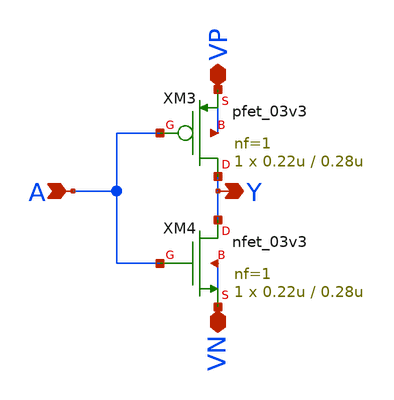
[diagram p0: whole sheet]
** sch_path: inverter/inverter.sch
**.subckt inverter A VP VN Y
*.ipin A
*.iopin VP
*.iopin VN
*.opin Y
XM3 Y A VP VP pfet_03v3 L=0.28u W=0.22u nf=1 ad='int((nf+1)/2) * W/nf * 0.18u' as='int((nf+2)/2) * W/nf * 0.18u'
+ pd='2*int((nf+1)/2) * (W/nf + 0.18u)' ps='2*int((nf+2)/2) * (W/nf + 0.18u)' nrd='0.18u / W' nrs='0.18u / W'
+ sa=0 sb=0 sd=0 m=1
XM4 Y A VN VN nfet_03v3 L=0.28u W=0.22u nf=1 ad='int((nf+1)/2) * W/nf * 0.18u' as='int((nf+2)/2) * W/nf * 0.18u'
+ pd='2*int((nf+1)/2) * (W/nf + 0.18u)' ps='2*int((nf+2)/2) * (W/nf + 0.18u)' nrd='0.18u / W' nrs='0.18u / W'
+ sa=0 sb=0 sd=0 m=1
**.ends
.end
